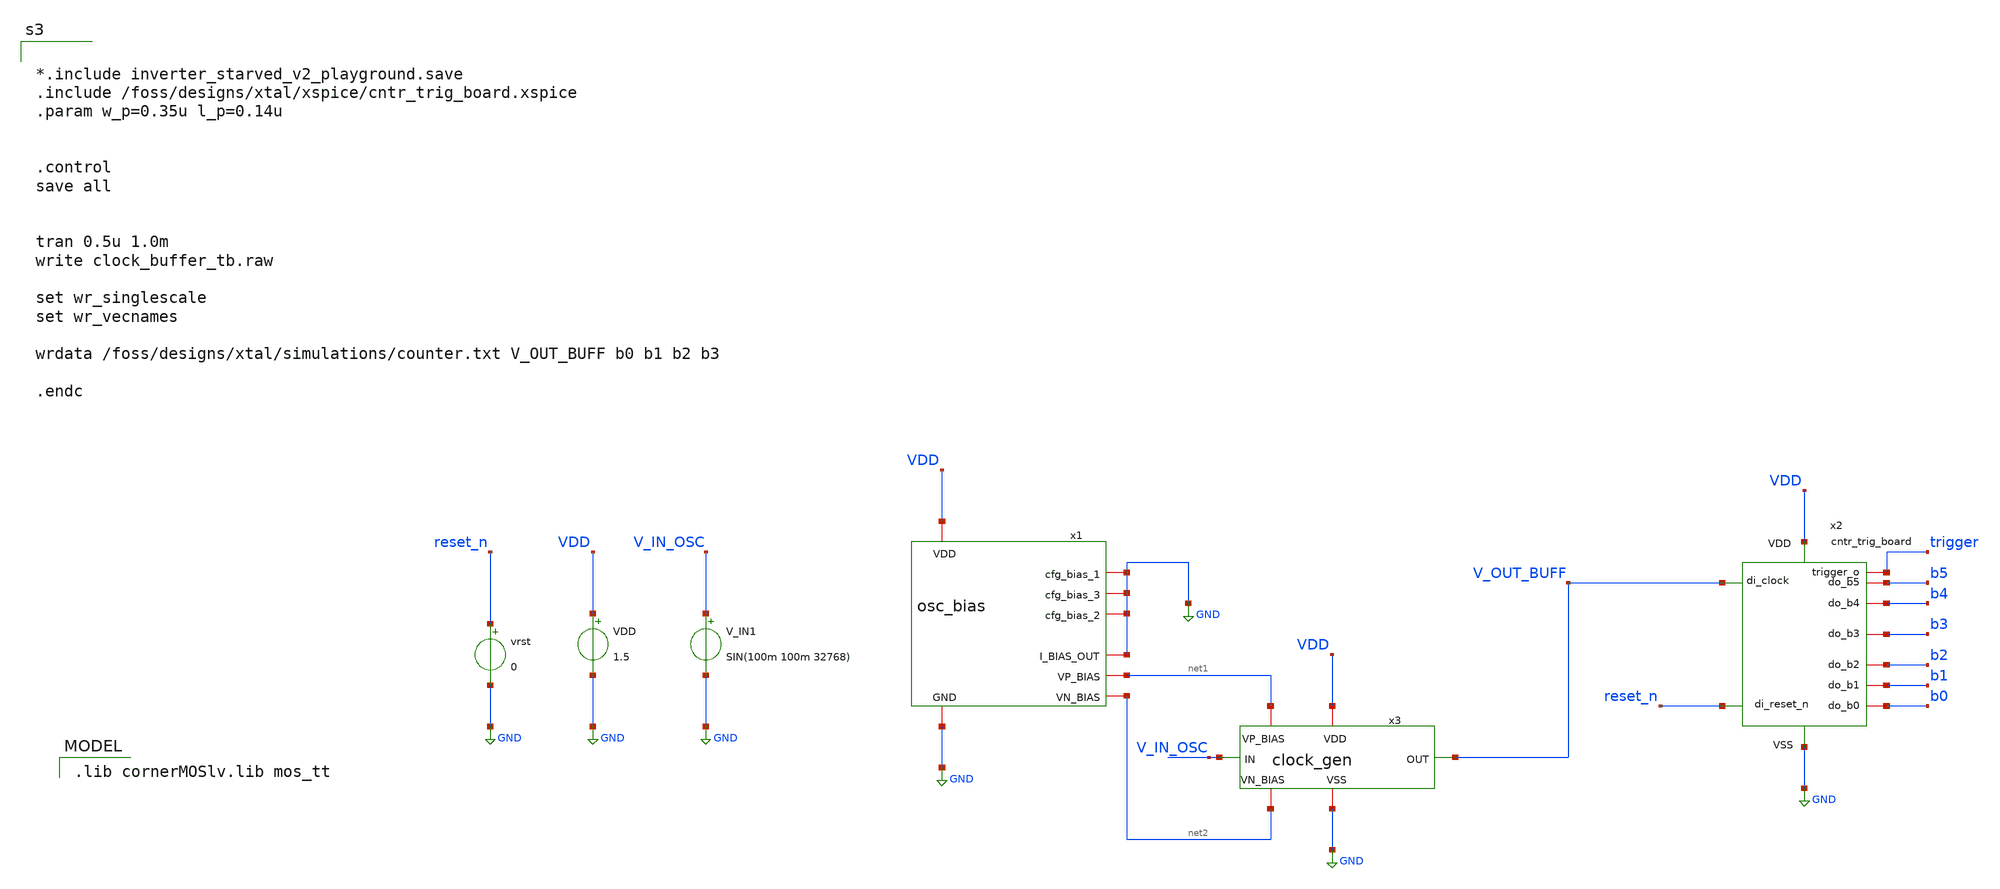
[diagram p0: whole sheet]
** sch_path: clock_buffer_tb.sch
**.subckt clock_buffer_tb
x1 VDD GND GND GND GND GND net1 net2 osc_bias
x2 VDD GND V_OUT_BUFF b0 b1 b2 b3 b4 b5 reset_n trigger cntr_trig_board
vrst reset_n GND 0
VDD VDD GND 1.5
x3 VDD V_IN_OSC V_OUT_BUFF GND net1 net2 clock_gen
V_IN1 V_IN_OSC GND SIN(100m 100m 32768)
**** begin user architecture code


*.include inverter_starved_v2_playground.save
.include /foss/designs/xtal/xspice/cntr_trig_board.xspice
.param w_p=0.35u l_p=0.14u


.control
save all


tran 0.5u 1.0m
write clock_buffer_tb.raw

set wr_singlescale
set wr_vecnames

wrdata /foss/designs/xtal/simulations/counter.txt V_OUT_BUFF b0 b1 b2 b3

.endc


 .lib cornerMOSlv.lib mos_tt

**** end user architecture code
**.ends

* expanding   symbol:  osc_bias.sym # of pins=8
** sym_path: osc_bias.sym
** sch_path: osc_bias.sch
.subckt osc_bias VDD cfg_bias_1 cfg_bias_3 cfg_bias_2 GND I_BIAS_OUT VP_BIAS VN_BIAS
*.iopin VDD
*.iopin GND
*.iopin I_BIAS_OUT
*.iopin cfg_bias_1
*.iopin cfg_bias_2
*.iopin cfg_bias_3
*.opin VN_BIAS
*.opin VP_BIAS
XM1 VP_BIAS VP_BIAS VDD VDD sg13_lv_pmos w=1u l=10u ng=1 m=1 mm_ok=1
XM3 VP_BIAS VP_BIAS net1 VN_BIAS sg13_lv_nmos w=0.25u l=10u ng=1 m=1 mm_ok=1
XM4 net1 net1 net2 VN_BIAS sg13_lv_nmos w=0.25u l=10u ng=1 m=1 mm_ok=1
XM5 net2 net2 VN_BIAS VN_BIAS sg13_lv_nmos w=0.25u l=10u ng=1 m=1 mm_ok=1
XM2 net6 VP_BIAS VDD VDD sg13_lv_pmos w=0.5u l=10u ng=1 m=1 mm_ok=1
XM6 I_BIAS_OUT cfg_bias_1 net6 VDD sg13_lv_pmos w=0.5u l=5u ng=1 m=1 mm_ok=1
XM7 net3 VP_BIAS VDD VDD sg13_lv_pmos w=0.5u l=10u ng=1 m=1 mm_ok=1
XM8 net4 VP_BIAS VDD VDD sg13_lv_pmos w=0.5u l=10u ng=1 m=1 mm_ok=1
XM9 I_BIAS_OUT cfg_bias_2 net3 VDD sg13_lv_pmos w=0.5u l=10u ng=1 m=1 mm_ok=1
XM10 I_BIAS_OUT cfg_bias_3 net4 VDD sg13_lv_pmos w=0.5u l=10u ng=1 m=1 mm_ok=1
XM11 VN_BIAS VN_BIAS net5 VN_BIAS sg13_lv_nmos w=0.25u l=10u ng=1 m=1 mm_ok=1
Vmeas net5 GND 0
.save i(vmeas)
.ends


* expanding   symbol:  clock_gen.sym # of pins=6
** sym_path: clock_gen.sym
** sch_path: clock_gen.sch
.subckt clock_gen VDD IN OUT VSS VP_BIAS VN_BIAS
*.ipin IN
*.iopin VSS
*.opin OUT
*.iopin VDD
*.ipin VP_BIAS
*.ipin VN_BIAS
XM13 V_OUT_1 V_IN_1 net2 VSS sg13_lv_nmos w={w_p} l={l_p} ng=1 m=1 mm_ok=1
XM14 V_OUT_1 V_IN_1 M2_Source VDD sg13_lv_pmos w={3*{w_p}} l={l_p} ng=1 m=1 mm_ok=1
XM15 net3 VN_BIAS VSS VSS sg13_lv_nmos w={w_p} l={l_p} ng=1 m=1 mm_ok=1
XM16 net1 VP_BIAS VDD VDD sg13_lv_pmos w={3*{w_p}} l={l_p} ng=1 m=1 mm_ok=1
Vmeas_PMOS1 net1 M2_Source 0
.save i(vmeas_pmos1)
Vmeas_NMOS1 net2 net3 0
.save i(vmeas_nmos1)
C2 IN V_IN_1 110p m=1
XM17 V_OUT_2 V_OUT_1 net4 VSS sg13_lv_nmos w={w_p} l={l_p} ng=1 m=1 mm_ok=1
XM18 V_OUT_2 V_OUT_1 net6 VDD sg13_lv_pmos w={3*{w_p}} l={l_p} ng=1 m=1 mm_ok=1
Vmeas_NMOS2 net4 net7 0
.save i(vmeas_nmos2)
XM19 net5 VP_BIAS VDD VDD sg13_lv_pmos w={3*{w_p}} l={l_p} ng=1 m=1 mm_ok=1
Vmeas_PMOS2 net5 net6 0
.save i(vmeas_pmos2)
XM20 net7 VN_BIAS VSS VSS sg13_lv_nmos w={w_p} l={l_p} ng=1 m=1 mm_ok=1
XM21 OUT V_OUT_4 net9 VSS sg13_lv_nmos w={w_p} l={l_p} ng=1 m=1 mm_ok=1
XM22 OUT V_OUT_4 net8 VDD sg13_lv_pmos w={3*{w_p}} l={l_p} ng=1 m=1 mm_ok=1
Vmeas_PMOS_OUT VDD net8 0
.save i(vmeas_pmos_out)
Vmeas_NMOS_OUT net9 VSS 0
.save i(vmeas_nmos_out)
XM25 V_OUT_3 V_OUT_2 net10 VSS sg13_lv_nmos w={w_p} l={l_p} ng=1 m=1 mm_ok=1
XM26 V_OUT_3 V_OUT_2 net12 VDD sg13_lv_pmos w={3*{w_p}} l={l_p} ng=1 m=1 mm_ok=1
Vmeas_NMOS3 net10 net13 0
.save i(vmeas_nmos3)
XM27 net11 VP_BIAS VDD VDD sg13_lv_pmos w={3*{w_p}} l={l_p} ng=1 m=1 mm_ok=1
Vmeas_PMOS3 net11 net12 0
.save i(vmeas_pmos3)
XM28 net13 VN_BIAS VSS VSS sg13_lv_nmos w={w_p} l={l_p} ng=1 m=1 mm_ok=1
XM29 V_OUT_4 V_OUT_3 net14 VSS sg13_lv_nmos w={w_p} l={l_p} ng=1 m=1 mm_ok=1
XM30 V_OUT_4 V_OUT_3 net16 VDD sg13_lv_pmos w={3*{w_p}} l={l_p} ng=1 m=1 mm_ok=1
Vmeas_NMOS4 net14 net17 0
.save i(vmeas_nmos4)
XM31 net15 VP_BIAS VDD VDD sg13_lv_pmos w={3*{w_p}} l={l_p} ng=1 m=1 mm_ok=1
Vmeas_PMOS4 net15 net16 0
.save i(vmeas_pmos4)
XM32 net17 VN_BIAS VSS VSS sg13_lv_nmos w={w_p} l={l_p} ng=1 m=1 mm_ok=1
XM1 net18 V_OUT_1 V_OUT_1 V_OUT_1 sg13_lv_pmos w=0.5u l=2u ng=1 m=1 mm_ok=1
XM2 net18 V_IN_1 V_IN_1 V_IN_1 sg13_lv_pmos w=0.5u l=2u ng=1 m=1 mm_ok=1
.ends

.GLOBAL GND
.end
